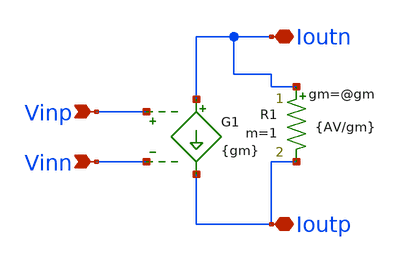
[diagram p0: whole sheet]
** sch_path: LPF design/SCLICAP_TEST/GM_cell.sch
**.subckt GM_cell Vinp Vinn Ioutn Ioutp
*.ipin Vinp
*.ipin Vinn
*.iopin Ioutn
*.iopin Ioutp
G1 Ioutn Ioutp Vinp Vinn {gm}
R1 Ioutn Ioutp {AV/gm} m=1
**.ends
.end
